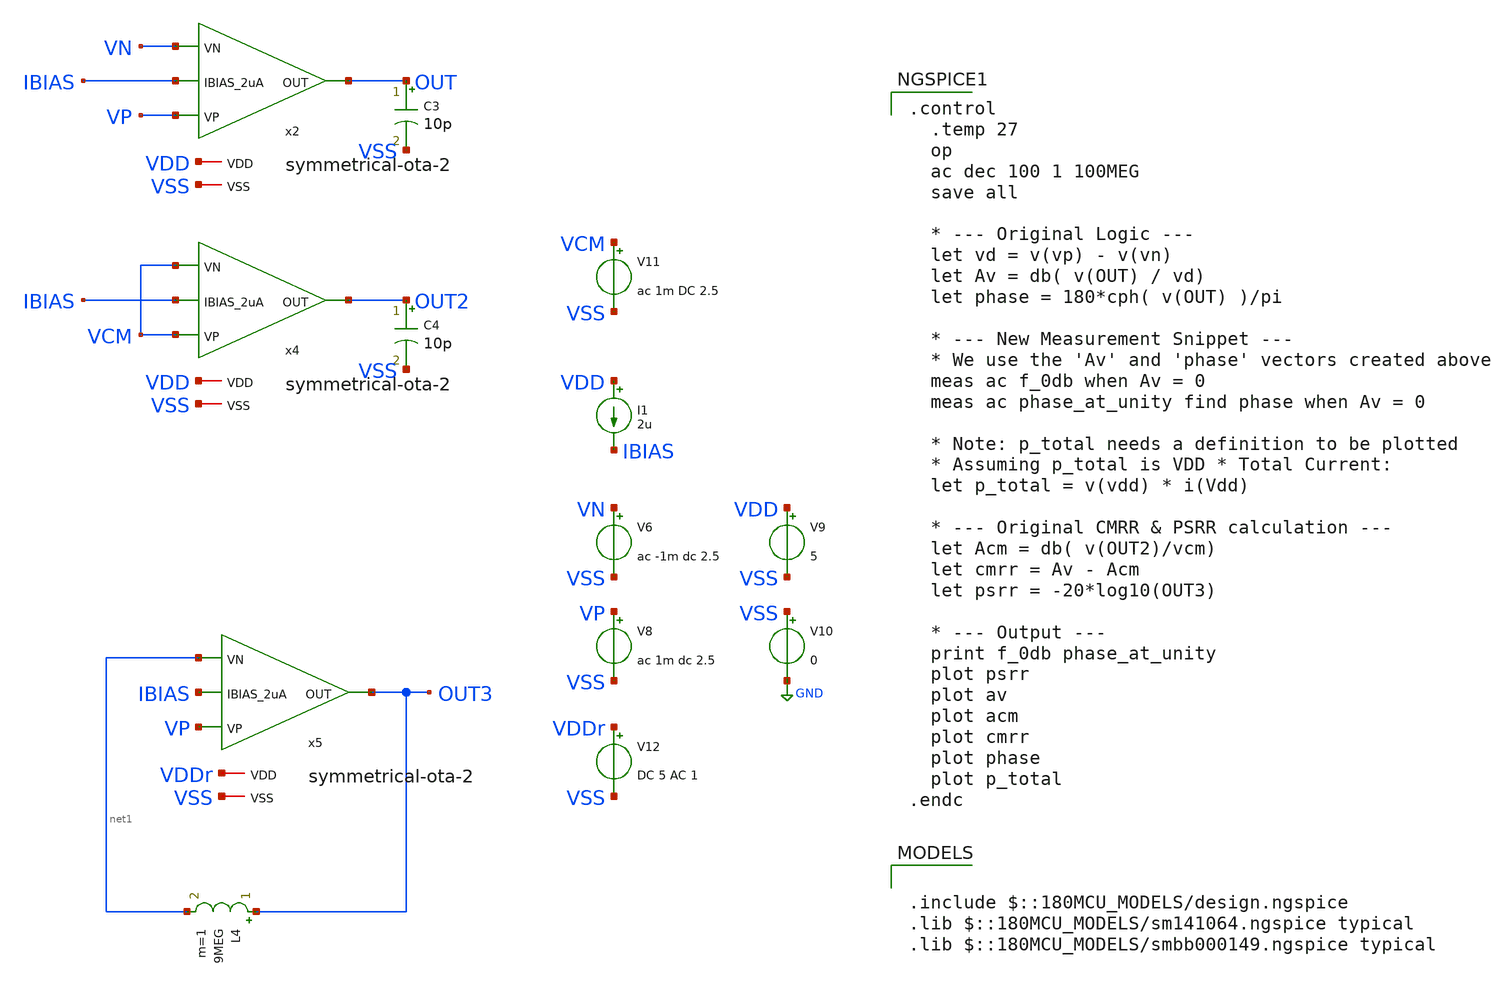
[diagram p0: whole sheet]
** sch_path: designs/symmetrical-ota-2/tb_ac.sch
**.subckt tb_ac
V6 VN VSS ac -1m dc 2.5
V8 VP VSS ac 1m dc 2.5
V9 VDD VSS 5
V10 VSS GND 0
C3 OUT VSS 10p m=1
I1 VDD IBIAS 2u
V11 VCM VSS ac 1m DC 2.5
V12 VDDr VSS DC 5 AC 1
L4 OUT3 net1 9MEG m=1
x2 VDD IBIAS OUT VN VP VSS symmetrical-ota-2
C4 OUT2 VSS 10p m=1
x4 VDD IBIAS OUT2 VCM VCM VSS symmetrical-ota-2
x5 VDDr IBIAS OUT3 net1 VP VSS symmetrical-ota-2
**** begin user architecture code

.control
  .temp 27
  op
  ac dec 100 1 100MEG
  save all

  * --- Original Logic ---
  let vd = v(vp) - v(vn)
  let Av = db( v(OUT) / vd)
  let phase = 180*cph( v(OUT) )/pi

  * --- New Measurement Snippet ---
  * We use the 'Av' and 'phase' vectors created above
  meas ac f_0db when Av = 0
  meas ac phase_at_unity find phase when Av = 0

  * Note: p_total needs a definition to be plotted
  * Assuming p_total is VDD * Total Current:
  let p_total = v(vdd) * i(Vdd)

  * --- Original CMRR & PSRR calculation ---
  let Acm = db( v(OUT2)/vcm)
  let cmrr = Av - Acm
  let psrr = -20*log10(OUT3)

  * --- Output ---
  print f_0db phase_at_unity
  plot psrr
  plot av
  plot acm
  plot cmrr
  plot phase
  plot p_total
.endc




.include $::180MCU_MODELS/design.ngspice
.lib $::180MCU_MODELS/sm141064.ngspice typical
.lib $::180MCU_MODELS/smbb000149.ngspice typical

**** end user architecture code
**.ends

* expanding   symbol:  symmetrical-ota-2.sym # of pins=6
** sym_path: designs/symmetrical-ota-2/symmetrical-ota-2.sym
** sch_path: designs/symmetrical-ota-2/symmetrical-ota-2.sch
.subckt symmetrical-ota-2 VDD IBIAS_2uA OUT VN VP VSS
*.iopin VDD
*.iopin VSS
*.opin OUT
*.ipin IBIAS_2uA
*.ipin VP
*.ipin VN
XM1 net1 VP net10 VDD pfet_05v0 L=3u W=53.5u nf=1 ad='int((nf+1)/2) * W/nf * 0.18u' as='int((nf+2)/2) * W/nf * 0.18u'
+ pd='2*int((nf+1)/2) * (W/nf + 0.18u)' ps='2*int((nf+2)/2) * (W/nf + 0.18u)' nrd='0.18u / W' nrs='0.18u / W'
+ sa=0 sb=0 sd=0 m=1
XM2 net2 VN net10 VDD pfet_05v0 L=3u W=53.4u nf=1 ad='int((nf+1)/2) * W/nf * 0.18u' as='int((nf+2)/2) * W/nf * 0.18u'
+ pd='2*int((nf+1)/2) * (W/nf + 0.18u)' ps='2*int((nf+2)/2) * (W/nf + 0.18u)' nrd='0.18u / W' nrs='0.18u / W'
+ sa=0 sb=0 sd=0 m=1
XM4 net2 net2 net3 VSS nfet_05v0 L=3u W=31.2u nf=1 ad='int((nf+1)/2) * W/nf * 0.18u' as='int((nf+2)/2) * W/nf * 0.18u'
+ pd='2*int((nf+1)/2) * (W/nf + 0.18u)' ps='2*int((nf+2)/2) * (W/nf + 0.18u)' nrd='0.18u / W' nrs='0.18u / W'
+ sa=0 sb=0 sd=0 m=1
XM6 net3 net3 VSS VSS nfet_05v0 L=3u W=31.2u nf=1 ad='int((nf+1)/2) * W/nf * 0.18u' as='int((nf+2)/2) * W/nf * 0.18u'
+ pd='2*int((nf+1)/2) * (W/nf + 0.18u)' ps='2*int((nf+2)/2) * (W/nf + 0.18u)' nrd='0.18u / W' nrs='0.18u / W'
+ sa=0 sb=0 sd=0 m=1
XM7 net1 net1 net4 VSS nfet_05v0 L=3u W=31.2u nf=1 ad='int((nf+1)/2) * W/nf * 0.18u' as='int((nf+2)/2) * W/nf * 0.18u'
+ pd='2*int((nf+1)/2) * (W/nf + 0.18u)' ps='2*int((nf+2)/2) * (W/nf + 0.18u)' nrd='0.18u / W' nrs='0.18u / W'
+ sa=0 sb=0 sd=0 m=1
XM8 net4 net4 VSS VSS nfet_05v0 L=3u W=31.2u nf=1 ad='int((nf+1)/2) * W/nf * 0.18u' as='int((nf+2)/2) * W/nf * 0.18u'
+ pd='2*int((nf+1)/2) * (W/nf + 0.18u)' ps='2*int((nf+2)/2) * (W/nf + 0.18u)' nrd='0.18u / W' nrs='0.18u / W'
+ sa=0 sb=0 sd=0 m=1
XM9 OUT net2 net6 VSS nfet_05v0 L=3u W=31.2u nf=1 ad='int((nf+1)/2) * W/nf * 0.18u' as='int((nf+2)/2) * W/nf * 0.18u'
+ pd='2*int((nf+1)/2) * (W/nf + 0.18u)' ps='2*int((nf+2)/2) * (W/nf + 0.18u)' nrd='0.18u / W' nrs='0.18u / W'
+ sa=0 sb=0 sd=0 m=1
XM10 net6 net3 VSS VSS nfet_05v0 L=3u W=31.2u nf=1 ad='int((nf+1)/2) * W/nf * 0.18u' as='int((nf+2)/2) * W/nf * 0.18u'
+ pd='2*int((nf+1)/2) * (W/nf + 0.18u)' ps='2*int((nf+2)/2) * (W/nf + 0.18u)' nrd='0.18u / W' nrs='0.18u / W'
+ sa=0 sb=0 sd=0 m=1
XM11 net8 net1 net5 VSS nfet_05v0 L=3u W=31.2u nf=1 ad='int((nf+1)/2) * W/nf * 0.18u' as='int((nf+2)/2) * W/nf * 0.18u'
+ pd='2*int((nf+1)/2) * (W/nf + 0.18u)' ps='2*int((nf+2)/2) * (W/nf + 0.18u)' nrd='0.18u / W' nrs='0.18u / W'
+ sa=0 sb=0 sd=0 m=1
XM12 net5 net4 VSS VSS nfet_05v0 L=3u W=31.2u nf=1 ad='int((nf+1)/2) * W/nf * 0.18u' as='int((nf+2)/2) * W/nf * 0.18u'
+ pd='2*int((nf+1)/2) * (W/nf + 0.18u)' ps='2*int((nf+2)/2) * (W/nf + 0.18u)' nrd='0.18u / W' nrs='0.18u / W'
+ sa=0 sb=0 sd=0 m=1
XM3 net8 net8 net7 VDD pfet_05v0 L=3u W=41.47u nf=1 ad='int((nf+1)/2) * W/nf * 0.18u' as='int((nf+2)/2) * W/nf * 0.18u'
+ pd='2*int((nf+1)/2) * (W/nf + 0.18u)' ps='2*int((nf+2)/2) * (W/nf + 0.18u)' nrd='0.18u / W' nrs='0.18u / W'
+ sa=0 sb=0 sd=0 m=1
XM5 OUT net8 net9 VDD pfet_05v0 L=3u W=41.47u nf=1 ad='int((nf+1)/2) * W/nf * 0.18u' as='int((nf+2)/2) * W/nf * 0.18u'
+ pd='2*int((nf+1)/2) * (W/nf + 0.18u)' ps='2*int((nf+2)/2) * (W/nf + 0.18u)' nrd='0.18u / W' nrs='0.18u / W'
+ sa=0 sb=0 sd=0 m=1
XM13 net7 net7 VDD VDD pfet_05v0 L=3u W=41.47u nf=1 ad='int((nf+1)/2) * W/nf * 0.18u' as='int((nf+2)/2) * W/nf * 0.18u'
+ pd='2*int((nf+1)/2) * (W/nf + 0.18u)' ps='2*int((nf+2)/2) * (W/nf + 0.18u)' nrd='0.18u / W' nrs='0.18u / W'
+ sa=0 sb=0 sd=0 m=1
XM14 net9 net7 VDD VDD pfet_05v0 L=3u W=41.47u nf=1 ad='int((nf+1)/2) * W/nf * 0.18u' as='int((nf+2)/2) * W/nf * 0.18u'
+ pd='2*int((nf+1)/2) * (W/nf + 0.18u)' ps='2*int((nf+2)/2) * (W/nf + 0.18u)' nrd='0.18u / W' nrs='0.18u / W'
+ sa=0 sb=0 sd=0 m=1
XM15 net10 net10 VDD VDD pfet_05v0 L=3u W=41.5u nf=1 ad='int((nf+1)/2) * W/nf * 0.18u' as='int((nf+2)/2) * W/nf * 0.18u'
+ pd='2*int((nf+1)/2) * (W/nf + 0.18u)' ps='2*int((nf+2)/2) * (W/nf + 0.18u)' nrd='0.18u / W' nrs='0.18u / W'
+ sa=0 sb=0 sd=0 m=1
XM16 IBIAS_2uA net10 VDD VDD pfet_05v0 L=3u W=41.5u nf=1 ad='int((nf+1)/2) * W/nf * 0.18u' as='int((nf+2)/2) * W/nf * 0.18u'
+ pd='2*int((nf+1)/2) * (W/nf + 0.18u)' ps='2*int((nf+2)/2) * (W/nf + 0.18u)' nrd='0.18u / W' nrs='0.18u / W'
+ sa=0 sb=0 sd=0 m=1
.ends

.GLOBAL GND
.end
